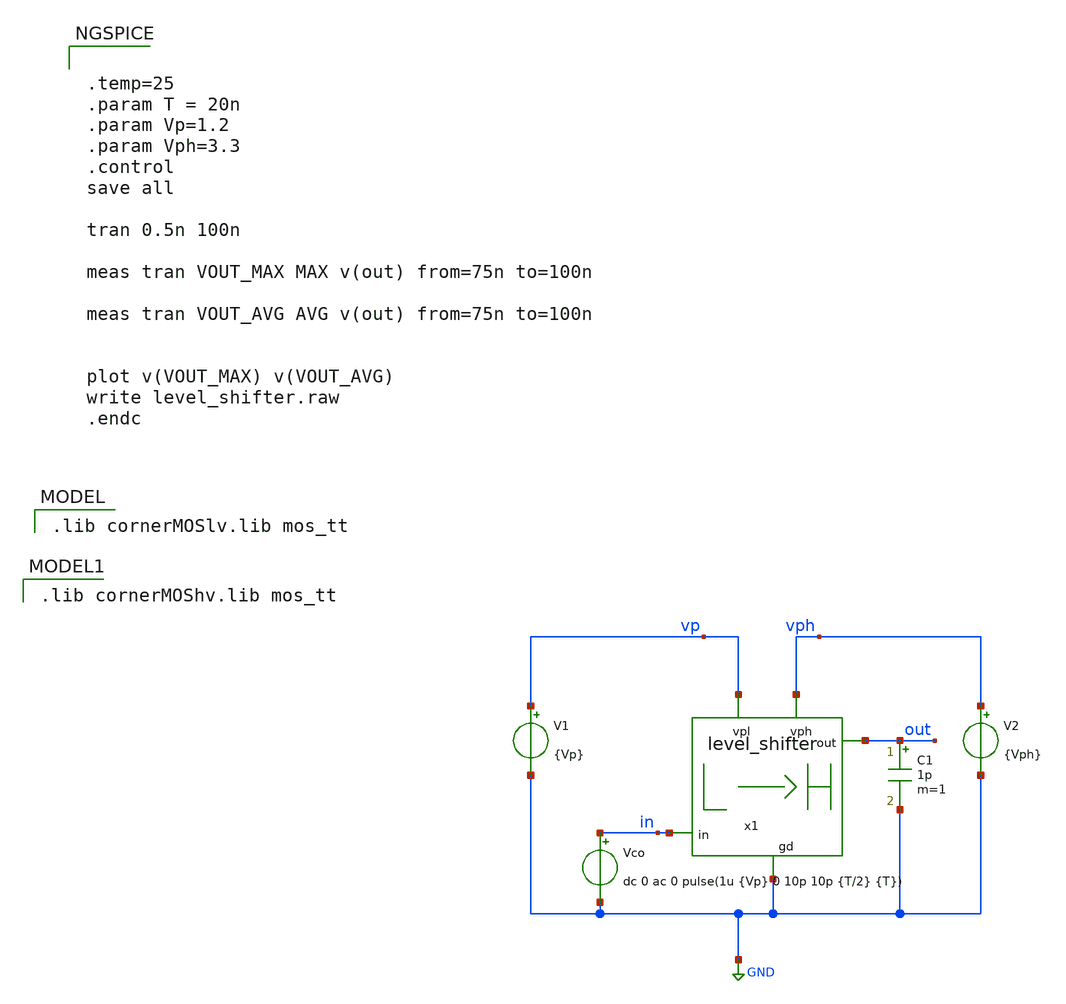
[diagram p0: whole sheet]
** sch_path: schematics/misc/level_shifter_tb.sch
**.subckt level_shifter_tb
x1 vph out vp in GND level_shifter
V1 vp GND {Vp}
V2 vph GND {Vph}
C1 out GND 1p m=1
Vco in GND dc 0 ac 0 pulse(1u {Vp} 0 10p 10p {T/2} {T})
**** begin user architecture code
 .lib cornerMOSlv.lib mos_tt



.temp=25
.param T = 20n
.param Vp=1.2
.param Vph=3.3
.control
save all

tran 0.5n 100n

meas tran VOUT_MAX MAX v(out) from=75n to=100n

meas tran VOUT_AVG AVG v(out) from=75n to=100n


plot v(VOUT_MAX) v(VOUT_AVG)
write level_shifter.raw
.endc


 .lib cornerMOShv.lib mos_tt

**** end user architecture code
**.ends

* expanding   symbol:  level_shifter.sym # of pins=5
** sym_path: schematics/misc/level_shifter.sym
** sch_path: schematics/misc/level_shifter.sch
.subckt level_shifter vph out vpl in gd
*.ipin in
*.opin out
*.ipin gd
*.ipin vph
*.ipin vpl
XM1 1_stage_out in vpl vpl sg13_lv_pmos w=2u l=0.45u ng=1 m=1 mm_ok=1
XM3 1_stage_out in net1 gd sg13_lv_nmos w=1u l=0.45u ng=1 m=1 mm_ok=1
XM4 net1 in gd gd sg13_lv_nmos w=1u l=0.45u ng=1 m=1 mm_ok=1
XM2 2_stage_out 1_stage_out vpl vpl sg13_lv_pmos w=2u l=0.45u ng=1 m=1 mm_ok=1
XM5 2_stage_out 1_stage_out net4 gd sg13_lv_nmos w=1u l=0.45u ng=1 m=1 mm_ok=1
XM6 net4 1_stage_out gd gd sg13_lv_nmos w=1u l=0.45u ng=1 m=1 mm_ok=1
XM7 net2 3_stage_out vph vph sg13_hv_pmos w=1u l=0.45u ng=1 m=1 mm_ok=1
XM8 3_stage_out 2_stage_out gd gd sg13_hv_nmos w=4u l=0.45u ng=1 m=1 mm_ok=1
XM9 4 1_stage_out net2 vph sg13_hv_pmos w=1u l=0.45u ng=1 m=1 mm_ok=1
XM10 3_stage_out 2_stage_out net3 vph sg13_hv_pmos w=2u l=0.45u ng=1 m=1 mm_ok=1
XM11 net3 4 vph vph sg13_hv_pmos w=2u l=0.45u ng=1 m=1 mm_ok=1
XM12 4 1_stage_out gd gd sg13_hv_nmos w=2u l=0.45u ng=1 m=1 mm_ok=1
XM15 buf_out_1 3_stage_out vph vph sg13_hv_pmos w=2u l=0.45u ng=1 m=1 mm_ok=1
XM14 buf_out_1 3_stage_out net5 gd sg13_hv_nmos w=1u l=0.45u ng=1 m=1 mm_ok=1
XM13 net5 3_stage_out gd gd sg13_hv_nmos w=1u l=0.45u ng=1 m=1 mm_ok=1
XM16 buf_out_2 buf_out_1 vph vph sg13_hv_pmos w=4u l=0.45u ng=1 m=2 mm_ok=1
XM17 buf_out_2 buf_out_1 net6 gd sg13_hv_nmos w=2u l=0.45u ng=1 m=2 mm_ok=1
XM18 net6 buf_out_1 gd gd sg13_hv_nmos w=2u l=0.45u ng=1 m=2 mm_ok=1
XM19 out buf_out_2 vph vph sg13_hv_pmos w=4u l=0.45u ng=1 m=8 mm_ok=1
XM20 out buf_out_2 net7 gd sg13_hv_nmos w=4u l=0.45u ng=1 m=4 mm_ok=1
XM21 net7 buf_out_2 gd gd sg13_hv_nmos w=4u l=0.45u ng=1 m=4 mm_ok=1
.ends

.GLOBAL GND
.end
